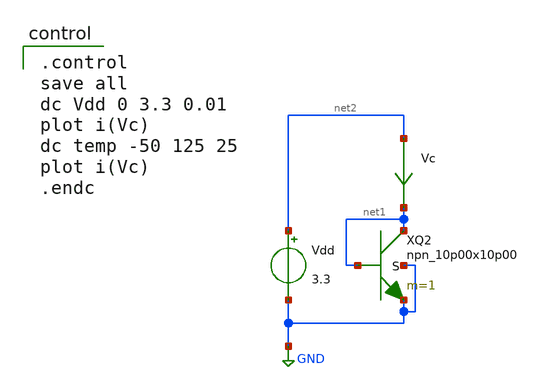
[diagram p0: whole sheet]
** sch_path: bgr/npn-diode.sch
**.subckt npn-diode
XQ2 net1 net1 GND GND npn_10p00x10p00 m=1
Vdd net2 GND 3.3
Vc net2 net1 0
.save i(vc)
**** begin user architecture code

.include $::180MCU_MODELS/design.ngspice
.lib $::180MCU_MODELS/sm141064.ngspice typical
.lib $::180MCU_MODELS/sm141064.ngspice res_typical
.lib $::180MCU_MODELS/sm141064.ngspice moscap_typical
.lib $::180MCU_MODELS/sm141064.ngspice bjt_typical
* .lib $::180MCU_MODELS/sm141064.ngspice res_statistical


.control
save all
dc Vdd 0 3.3 0.01
plot i(Vc)
dc temp -50 125 25
plot i(Vc)
.endc

**** end user architecture code
**.ends
.GLOBAL GND
.end
